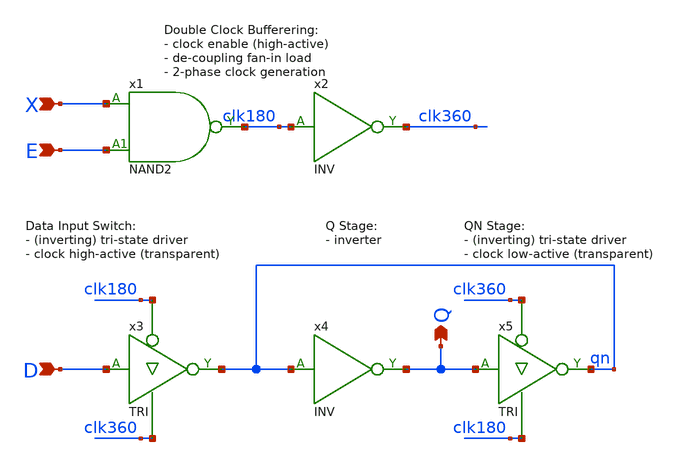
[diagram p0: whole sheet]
** sch_path: Sources/crafted/LATPE.sch
**.subckt LATPE X D Q E
*.ipin X
*.ipin D
*.opin Q
*.ipin E
x1 X E clk180 VDD GND NAND2 Wmin=1.5u Lmin=1u g=2 m=1
x2 clk180 clk360 VDD GND INV Wmin=1.5u Lmin=1u g=2 m=1
x3 D clk180 clk360 qn VDD GND TRI Wmin=1.5u Lmin=1u g=2 m=1
x5 Q clk360 clk180 qn VDD GND TRI Wmin=1.5u Lmin=1u g=2 m=1
x4 qn Q VDD GND INV Wmin=1.5u Lmin=1u g=2 m=1
**.ends
.end
